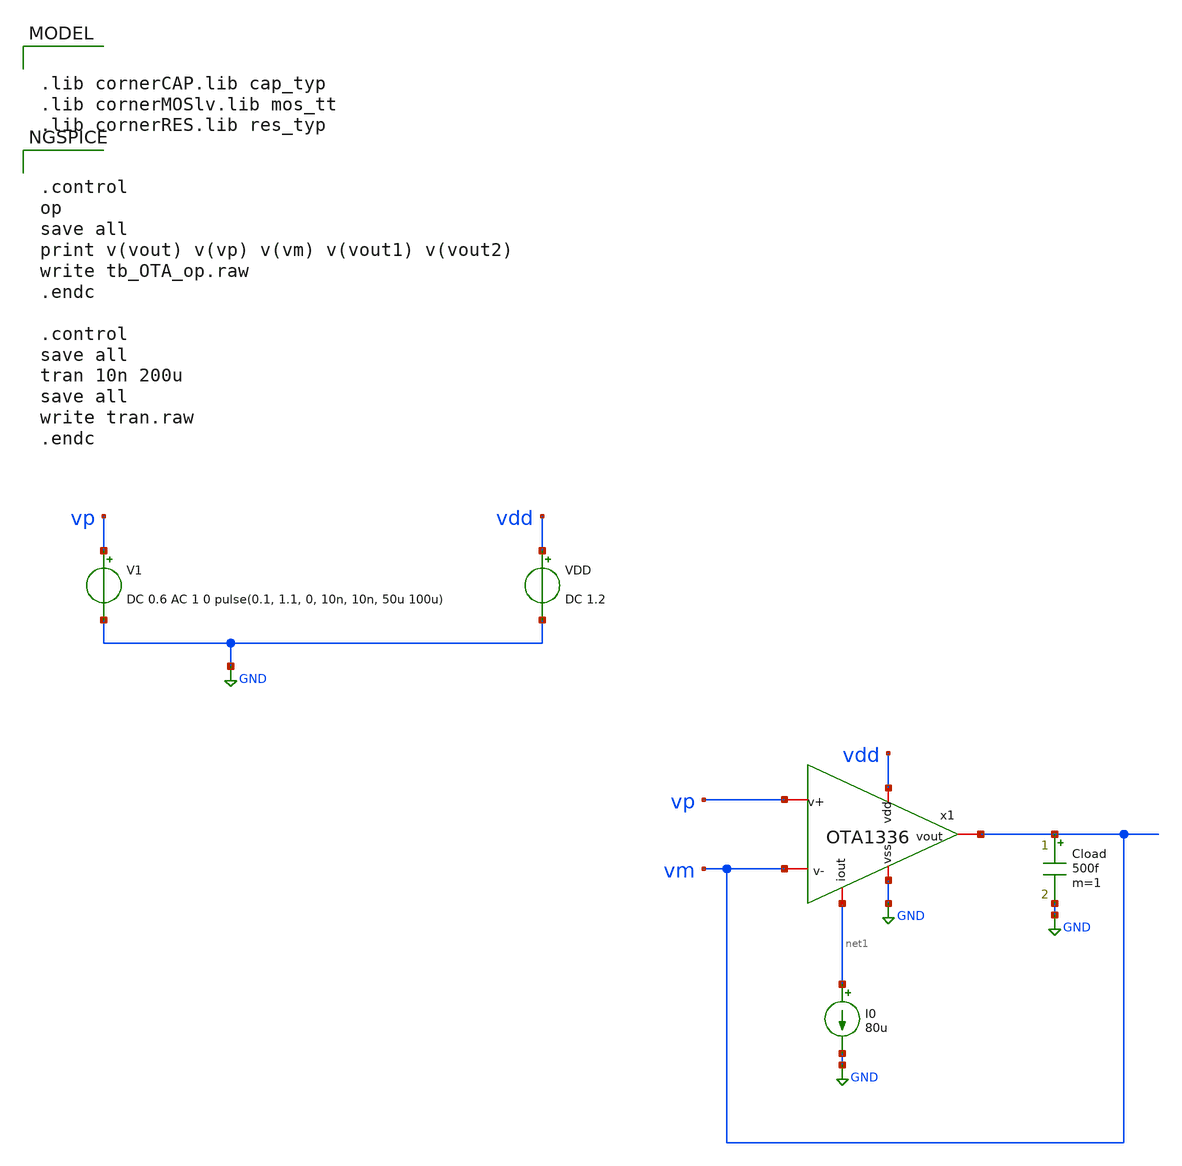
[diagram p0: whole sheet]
** sch_path: tests/data/OTA1336/testbenches/tran/xschem/OTA1336_tb.sch
**.subckt OTA1336_tb
V1 vp GND DC 0.6 AC 1 0 pulse(0.1, 1.1, 0, 10n, 10n, 50u 100u)
VDD vdd GND DC 1.2
I0 net1 GND 80u
Cload vm GND 500f m=1
x1 vdd net1 vm vm vp GND OTA1336
**** begin user architecture code

.lib cornerCAP.lib cap_typ
.lib cornerMOSlv.lib mos_tt
.lib cornerRES.lib res_typ



.control
op
save all
print v(vout) v(vp) v(vm) v(vout1) v(vout2)
write tb_OTA_op.raw
.endc

.control
save all
tran 10n 200u
save all
write tran.raw
.endc


**** end user architecture code
**.ends
.GLOBAL GND
.end
